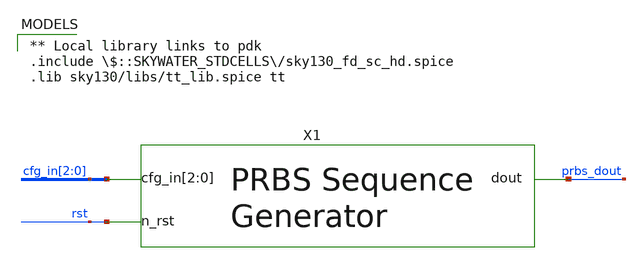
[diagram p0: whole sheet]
** sch_path: xschem/prb_gen_tb.sch
 ** Local library links to pdk
.include $::SKYWATER_STDCELLS/sky130_fd_sc_hd.spice
.lib sky130/libs/tt_lib.spice tt
**.subckt prb_gen_tb
X1 cfg_in[2] cfg_in[1] cfg_in[0] rst prbs_dout VDD GND prbs_gen
**.ends

* expanding   symbol:  xschem/prbs_gen.sym # of pins=3
** sym_path: xschem/prbs_gen.sym
** sch_path: xschem/prbs_gen.sch
.subckt prbs_gen cfg_in[2] cfg_in[1] cfg_in[0] n_rst dout VDD GND
*.ipin cfg_in[2],cfg_in[1],cfg_in[0]
*.opin dout
*.ipin n_rst
x8 net13 net6 GND GND VDD VDD net48 net6 sky130_fd_sc_hd__dfxbp_1
x16 net5 GND GND VDD VDD net14 sky130_fd_sc_hd__clkbuf_1
x5 net2 GND GND VDD VDD net3 sky130_fd_sc_hd__clkinv_1
x6 net3 GND GND VDD VDD net4 sky130_fd_sc_hd__clkinv_1
x7 net4 GND GND VDD VDD net5 sky130_fd_sc_hd__clkinv_1
x15 net14 GND GND VDD VDD net15 sky130_fd_sc_hd__clkbuf_1
x9 net6 net7 GND GND VDD VDD net49 net7 sky130_fd_sc_hd__dfxbp_1
x10 net7 net8 GND GND VDD VDD net50 net8 sky130_fd_sc_hd__dfxbp_1
x11 net8 net9 GND GND VDD VDD net51 net9 sky130_fd_sc_hd__dfxbp_1
x12 net9 net10 GND GND VDD VDD net52 net10 sky130_fd_sc_hd__dfxbp_1
x13 net10 net11 GND GND VDD VDD net53 net11 sky130_fd_sc_hd__dfxbp_1
x14 net11 net12 GND GND VDD VDD net54 net12 sky130_fd_sc_hd__dfxbp_1
x1 net15 GND GND VDD VDD net16 sky130_fd_sc_hd__clkbuf_1
x2 net16 GND GND VDD VDD net13 sky130_fd_sc_hd__clkbuf_1
x3 net17 GND GND VDD VDD net2 sky130_fd_sc_hd__clkinv_1
x4 net1 GND GND VDD VDD net17 sky130_fd_sc_hd__clkinv_1
x17 clk_0 clken_0 GND GND VDD VDD clk_sel sky130_fd_sc_hd__einvn_4
x19 cfg_in[2] cfg_in[0] cfg_in[1] GND GND VDD VDD clken_0 sky130_fd_sc_hd__or3_1
x25 cfg_in[2] cfg_in[1] cfg_in[0] GND GND VDD VDD clken_1 sky130_fd_sc_hd__or3b_1
x26 net13 GND GND VDD VDD clk_0 sky130_fd_sc_hd__clkbuf_1
x28 net6 GND GND VDD VDD clk_1 sky130_fd_sc_hd__clkbuf_1
x29 net7 GND GND VDD VDD clk_2 sky130_fd_sc_hd__clkbuf_1
x30 net8 GND GND VDD VDD clk_3 sky130_fd_sc_hd__clkbuf_1
x31 net9 GND GND VDD VDD clk_4 sky130_fd_sc_hd__clkbuf_1
x32 net10 GND GND VDD VDD clk_5 sky130_fd_sc_hd__clkbuf_1
x33 net11 GND GND VDD VDD clk_6 sky130_fd_sc_hd__clkbuf_1
x34 net12 GND GND VDD VDD clk_7 sky130_fd_sc_hd__clkbuf_1
x20 cfg_in[2] cfg_in[0] cfg_in[1] GND GND VDD VDD clken_2 sky130_fd_sc_hd__or3b_1
x21 cfg_in[2] cfg_in[0] cfg_in[1] GND GND VDD VDD clken_3 sky130_fd_sc_hd__nand3b_1
x22 cfg_in[1] cfg_in[0] cfg_in[2] GND GND VDD VDD clken_4 sky130_fd_sc_hd__or3b_1
x23 cfg_in[1] cfg_in[0] cfg_in[2] GND GND VDD VDD clken_5 sky130_fd_sc_hd__nand3b_1
x35 cfg_in[0] cfg_in[1] cfg_in[2] GND GND VDD VDD clken_6 sky130_fd_sc_hd__nand3b_1
x36 cfg_in[0] cfg_in[2] cfg_in[1] GND GND VDD VDD clken_7 sky130_fd_sc_hd__nand3_1
x18 clk_1 clken_1 GND GND VDD VDD clk_sel sky130_fd_sc_hd__einvn_1
x24 clk_2 clken_2 GND GND VDD VDD clk_sel sky130_fd_sc_hd__einvn_1
x27 clk_3 clken_3 GND GND VDD VDD clk_sel sky130_fd_sc_hd__einvn_1
x37 clk_4 clken_4 GND GND VDD VDD clk_sel sky130_fd_sc_hd__einvn_1
x38 clk_5 clken_5 GND GND VDD VDD clk_sel sky130_fd_sc_hd__einvn_1
x39 clk_6 clken_6 GND GND VDD VDD clk_sel sky130_fd_sc_hd__einvn_1
x40 clk_7 clken_7 GND GND VDD VDD clk_sel sky130_fd_sc_hd__einvn_1
x41 clk_sel GND GND VDD VDD net47 sky130_fd_sc_hd__clkinv_1
x42 net18 GND GND VDD VDD net1 sky130_fd_sc_hd__clkinv_1
x43 net5 GND GND VDD VDD net18 sky130_fd_sc_hd__clkinv_1
xsr_0 clk_out dout n_rst GND GND VDD VDD lfsr_0 sky130_fd_sc_hd__dfstp_1
x44 lfsr_0 lfsr_31 lfsr_28 GND GND VDD VDD dout sky130_fd_sc_hd__xor3_1
xsr_1 clk_out lfsr_0 GND GND VDD VDD net19 sky130_fd_sc_hd__dfxtp_1
xsr_2 clk_out net19 GND GND VDD VDD net20 sky130_fd_sc_hd__dfxtp_1
xsr_3 clk_out net20 GND GND VDD VDD net21 sky130_fd_sc_hd__dfxtp_1
xsr_4 clk_out net21 GND GND VDD VDD net22 sky130_fd_sc_hd__dfxtp_1
xsr_5 clk_out net22 GND GND VDD VDD net23 sky130_fd_sc_hd__dfxtp_1
xsr_6 clk_out net23 GND GND VDD VDD net24 sky130_fd_sc_hd__dfxtp_1
xsr_7 clk_out net24 GND GND VDD VDD net44 sky130_fd_sc_hd__dfxtp_1
xsr_8 clk_out net44 GND GND VDD VDD net25 sky130_fd_sc_hd__dfxtp_1
xsr_9 clk_out net25 GND GND VDD VDD net26 sky130_fd_sc_hd__dfxtp_1
xsr_10 clk_out net26 GND GND VDD VDD net27 sky130_fd_sc_hd__dfxtp_1
xsr_11 clk_out net27 GND GND VDD VDD net28 sky130_fd_sc_hd__dfxtp_1
xsr_12 clk_out net28 GND GND VDD VDD net29 sky130_fd_sc_hd__dfxtp_1
xsr_13 clk_out net29 GND GND VDD VDD net30 sky130_fd_sc_hd__dfxtp_1
xsr_14 clk_out net30 GND GND VDD VDD net31 sky130_fd_sc_hd__dfxtp_1
xsr_15 clk_out net31 GND GND VDD VDD net45 sky130_fd_sc_hd__dfxtp_1
xsr_16 clk_out net45 GND GND VDD VDD net32 sky130_fd_sc_hd__dfxtp_1
xsr_17 clk_out net32 GND GND VDD VDD net33 sky130_fd_sc_hd__dfxtp_1
xsr_18 clk_out net33 GND GND VDD VDD net34 sky130_fd_sc_hd__dfxtp_1
xsr_19 clk_out net34 GND GND VDD VDD net35 sky130_fd_sc_hd__dfxtp_1
xsr_20 clk_out net35 GND GND VDD VDD net36 sky130_fd_sc_hd__dfxtp_1
xsr_21 clk_out net36 GND GND VDD VDD net37 sky130_fd_sc_hd__dfxtp_1
xsr_22 clk_out net37 GND GND VDD VDD net38 sky130_fd_sc_hd__dfxtp_1
xsr_23 clk_out net38 GND GND VDD VDD net46 sky130_fd_sc_hd__dfxtp_1
xsr_24 clk_out net46 GND GND VDD VDD net39 sky130_fd_sc_hd__dfxtp_1
xsr_25 clk_out net39 GND GND VDD VDD net40 sky130_fd_sc_hd__dfxtp_1
xsr_26 clk_out net40 GND GND VDD VDD net41 sky130_fd_sc_hd__dfxtp_1
xsr_27 clk_out net41 GND GND VDD VDD lfsr_28 sky130_fd_sc_hd__dfxtp_1
xsr_28 clk_out lfsr_28 GND GND VDD VDD net42 sky130_fd_sc_hd__dfxtp_1
xsr_29 clk_out net42 GND GND VDD VDD net43 sky130_fd_sc_hd__dfxtp_1
xsr_30 clk_out net43 GND GND VDD VDD lfsr_31 sky130_fd_sc_hd__dfxtp_1
x46 net47 GND GND VDD VDD clk_out sky130_fd_sc_hd__clkinv_4
.ends

**** begin user architecture code


* power voltage
vvdd VDD 0 1.5

** STATIC CONTOL


** Signal
vcfg2 cfg_in[2]  0  0
vcfg1 cfg_in[1]  0  0
vcfg0 cfg_in[0]  0  0

vrst rst 0 0 PWL 0 0 19.990ns 0 20ns 1.5



.control
save all
set temp=27
set num_threads=6

* RUN SIMULATION
tran 1p 200n

* OUTPUT
set hcopydevtype = svg
hardcopy ./prbs_tb.svg   x1.clk_out prbs_dout+2 rst+2 title 'PRBS Output'
hardcopy ./prbs_clks.svg x1.clken_0 x1.clken_1+2 x1.clken_2+4 x1.clken_3+6 x1.clken_4+8 x1.clken_5+10
+ x1.clken_6+12 x1.clken_7+14 title 'prbs clkens'

.endc


**** end user architecture code
.end
